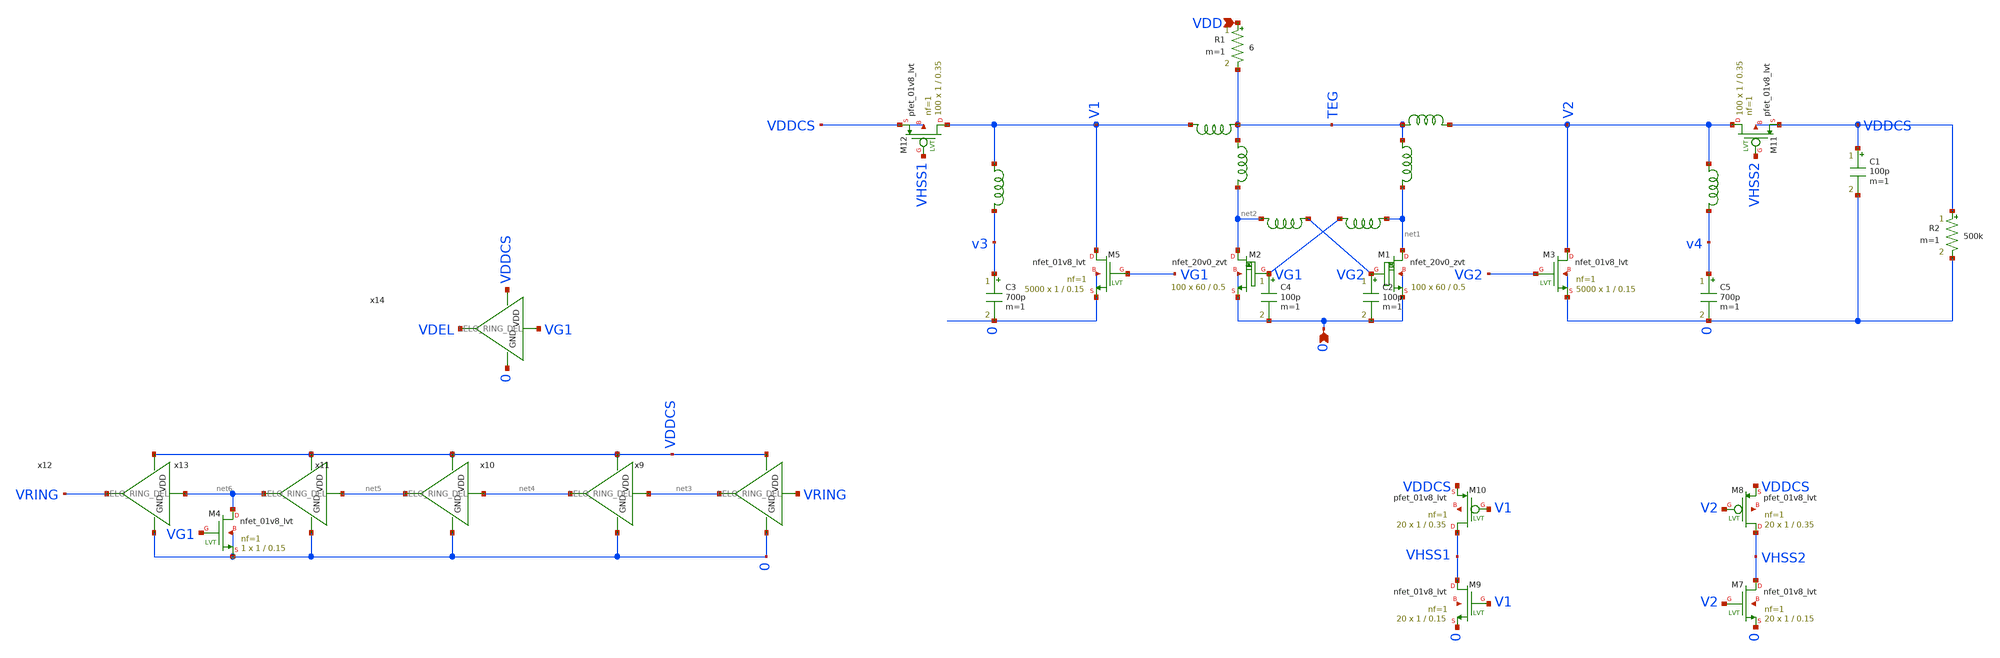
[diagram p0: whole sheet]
** sch_path: design/LELO_SVOD_SKY130A/LELO_EXSC.sch
**.subckt LELO_EXSC 0 VDD
*.ipin 0
*.ipin VDD
XM1 net1 VG2 0 0 sky130_fd_pr__nfet_20v0_zvt W=60 L=0.5 m=100
XM2 net2 VG1 0 0 sky130_fd_pr__nfet_20v0_zvt W=60 L=0.5 m=100
C1 VDDCS 0 100p m=1
C2 VG2 0 100p m=1
R1 VDD TEG 6 m=1
XM3 V2 VG2 0 0 sky130_fd_pr__nfet_01v8_lvt L=0.15 W=1 nf=1 ad='int((1 + 1)/2) * 1 / 1 * 0.29' as='int((1 + 2)/2) * 1 / 1 * 0.29'
+ pd='2*int((1 + 1)/2) * (1 / 1 + 0.29)' ps='2*int((1 + 2)/2) * (1 / 1 + 0.29)' nrd='0.29 / 1 ' nrs='0.29 / 1 '
+ sa=0 sb=0 sd=0 mult=5000 m=5000
XM5 V1 VG1 0 0 sky130_fd_pr__nfet_01v8_lvt L=0.15 W=1 nf=1 ad='int((1 + 1)/2) * 1 / 1 * 0.29' as='int((1 + 2)/2) * 1 / 1 * 0.29'
+ pd='2*int((1 + 1)/2) * (1 / 1 + 0.29)' ps='2*int((1 + 2)/2) * (1 / 1 + 0.29)' nrd='0.29 / 1 ' nrs='0.29 / 1 '
+ sa=0 sb=0 sd=0 mult=5000 m=5000
x1 VG2 net2 1812PS-564_imp
x2 net1 VG1 1812PS-564_imp
C4 VG1 0 100p m=1
x7 TEG V1 1812PS-103_imp
x8 TEG V2 1812PS-103_imp
R2 VDDCS 0 500k m=1
x3 TEG net2 1812PS-103_imp
x4 TEG net1 1812PS-103_imp
x5 V1 v3 1812PS-473_imp
C3 v3 0 700p m=1
C5 v4 0 700p m=1
x6 V2 v4 1812PS-473_imp
XM7 VHSS2 V2 0 net7 sky130_fd_pr__nfet_01v8_lvt L=0.15 W=1 nf=1 ad='int((1 + 1)/2) * 1 / 1 * 0.29' as='int((1 + 2)/2) * 1 / 1 * 0.29'
+ pd='2*int((1 + 1)/2) * (1 / 1 + 0.29)' ps='2*int((1 + 2)/2) * (1 / 1 + 0.29)' nrd='0.29 / 1 ' nrs='0.29 / 1 '
+ sa=0 sb=0 sd=0 mult=20 m=20
XM8 VHSS2 V2 VDDCS net8 sky130_fd_pr__pfet_01v8_lvt L=0.35 W=1 nf=1 ad='int((1 + 1)/2) * 1 / 1 * 0.29'
+ as='int((1 + 2)/2) * 1 / 1 * 0.29' pd='2*int((1 + 1)/2) * (1 / 1 + 0.29)' ps='2*int((1 + 2)/2) * (1 / 1 + 0.29)'
+ nrd='0.29 / 1 ' nrs='0.29 / 1 ' sa=0 sb=0 sd=0 mult=20 m=20
XM9 VHSS1 V1 0 net9 sky130_fd_pr__nfet_01v8_lvt L=0.15 W=1 nf=1 ad='int((1 + 1)/2) * 1 / 1 * 0.29' as='int((1 + 2)/2) * 1 / 1 * 0.29'
+ pd='2*int((1 + 1)/2) * (1 / 1 + 0.29)' ps='2*int((1 + 2)/2) * (1 / 1 + 0.29)' nrd='0.29 / 1 ' nrs='0.29 / 1 '
+ sa=0 sb=0 sd=0 mult=20 m=20
XM10 VHSS1 V1 VDDCS net10 sky130_fd_pr__pfet_01v8_lvt L=0.35 W=1 nf=1 ad='int((1 + 1)/2) * 1 / 1 * 0.29'
+ as='int((1 + 2)/2) * 1 / 1 * 0.29' pd='2*int((1 + 1)/2) * (1 / 1 + 0.29)' ps='2*int((1 + 2)/2) * (1 / 1 + 0.29)'
+ nrd='0.29 / 1 ' nrs='0.29 / 1 ' sa=0 sb=0 sd=0 mult=20 m=20
XM11 V2 VHSS2 VDDCS VDDCS sky130_fd_pr__pfet_01v8_lvt L=0.35 W=1 nf=1 ad='int((1 + 1)/2) * 1 / 1 * 0.29'
+ as='int((1 + 2)/2) * 1 / 1 * 0.29' pd='2*int((1 + 1)/2) * (1 / 1 + 0.29)' ps='2*int((1 + 2)/2) * (1 / 1 + 0.29)'
+ nrd='0.29 / 1 ' nrs='0.29 / 1 ' sa=0 sb=0 sd=0 mult=100 m=100
XM12 V1 VHSS1 VDDCS VDDCS sky130_fd_pr__pfet_01v8_lvt L=0.35 W=1 nf=1 ad='int((1 + 1)/2) * 1 / 1 * 0.29'
+ as='int((1 + 2)/2) * 1 / 1 * 0.29' pd='2*int((1 + 1)/2) * (1 / 1 + 0.29)' ps='2*int((1 + 2)/2) * (1 / 1 + 0.29)'
+ nrd='0.29 / 1 ' nrs='0.29 / 1 ' sa=0 sb=0 sd=0 mult=100 m=100
x9 VDDCS VRING net3 0 LELO_RING_DEL
x10 VDDCS net3 net4 0 LELO_RING_DEL
x11 VDDCS net4 net5 0 LELO_RING_DEL
x12 VDDCS net6 VRING 0 LELO_RING_DEL
x13 VDDCS net5 net6 0 LELO_RING_DEL
XM4 net6 VG1 0 0 sky130_fd_pr__nfet_01v8_lvt L=0.15 W=1 nf=1 ad='int((1 + 1)/2) * 1 / 1 * 0.29' as='int((1 + 2)/2) * 1 / 1 * 0.29'
+ pd='2*int((1 + 1)/2) * (1 / 1 + 0.29)' ps='2*int((1 + 2)/2) * (1 / 1 + 0.29)' nrd='0.29 / 1 ' nrs='0.29 / 1 '
+ sa=0 sb=0 sd=0 mult=1 m=1
x14 VDDCS VG1 VDEL 0 LELO_RING_DEL
**.ends

* expanding   symbol:  LELO_SVOD_SKY130A/1812PS-564_imp.sym # of pins=2
** sym_path: design/LELO_SVOD_SKY130A/1812PS-564_imp.sym

.subckt 1812PS-564_imp port1 port2
X1 port1 port2 Model1D R1=70 R2=6.1 C= 7.71p K1=0.000001 K2=115.8 K3= 560u K4=0.000001 K5=0.000001
+ L=0 Is=0 a=0 L_Z0=0 L_EL=0 L_F0=0E6 PkZ=153558.837
.ends 1812PS-564_imp

* expanding   symbol:  LELO_SVOD_SKY130A/1812PS-103_imp.sym # of pins=2
** sym_path: design/LELO_SVOD_SKY130A/1812PS-103_imp.sym

.subckt 1812PS-103_imp port1 port2
X1 port1 port2 Model1D R1=29 R2=0.17 C= 0.28p K1=0.000001 K2=0.741 K3= 10u K4=0.0014 K5=0.0000509
+ L=0 Is=0 a=0 L_Z0=0 L_EL=0 L_F0=0E6 PkZ=7186.74953
.ends 1812PS-103_imp

* expanding   symbol:  LELO_SVOD_SKY130A/1812PS-473_imp.sym # of pins=2
** sym_path: design/LELO_SVOD_SKY130A/1812PS-473_imp.sym

.subckt 1812PS-473_imp port1 port2
X1 port1 port2 Model1D R1=30 R2=0.87 C= 0.767p K1=0.000001 K2=4.63 K3= 47u K4=0.647 K5=0.00000972
+ L=0 Is=0 a=0 L_Z0=0 L_EL=0 L_F0=0E6 PkZ=23517.1382
.ends 1812PS-473_imp

* expanding   symbol:  LELO_SVOD_SKY130A/LELO_RING_DEL.sym # of pins=4
** sym_path: design/LELO_SVOD_SKY130A/LELO_RING_DEL.sym
** sch_path: design/LELO_SVOD_SKY130A/LELO_RING_DEL.sch
.subckt LELO_RING_DEL VDD VIN VOUT GND
*.ipin VIN
*.ipin VDD
*.ipin GND
*.opin VOUT
XM1 VOUT VIN GND GND sky130_fd_pr__nfet_01v8_lvt L=3 W=0.42 nf=1 ad='int((1 + 1)/2) * 0.42 / 1 * 0.29'
+ as='int((1 + 2)/2) * 0.42 / 1 * 0.29' pd='2*int((1 + 1)/2) * (0.42 / 1 + 0.29)' ps='2*int((1 + 2)/2) * (0.42 / 1 + 0.29)'
+ nrd='0.29 / 0.42 ' nrs='0.29 / 0.42 ' sa=0 sb=0 sd=0 mult=1 m=1
XM2 VOUT VIN VDD VDD sky130_fd_pr__pfet_01v8_lvt L=2.5 W=0.42 nf=1 ad='int((1 + 1)/2) * 0.42 / 1 * 0.29'
+ as='int((1 + 2)/2) * 0.42 / 1 * 0.29' pd='2*int((1 + 1)/2) * (0.42 / 1 + 0.29)' ps='2*int((1 + 2)/2) * (0.42 / 1 + 0.29)'
+ nrd='0.29 / 0.42 ' nrs='0.29 / 0.42 ' sa=0 sb=0 sd=0 mult=1 m=1
.ends

.end
